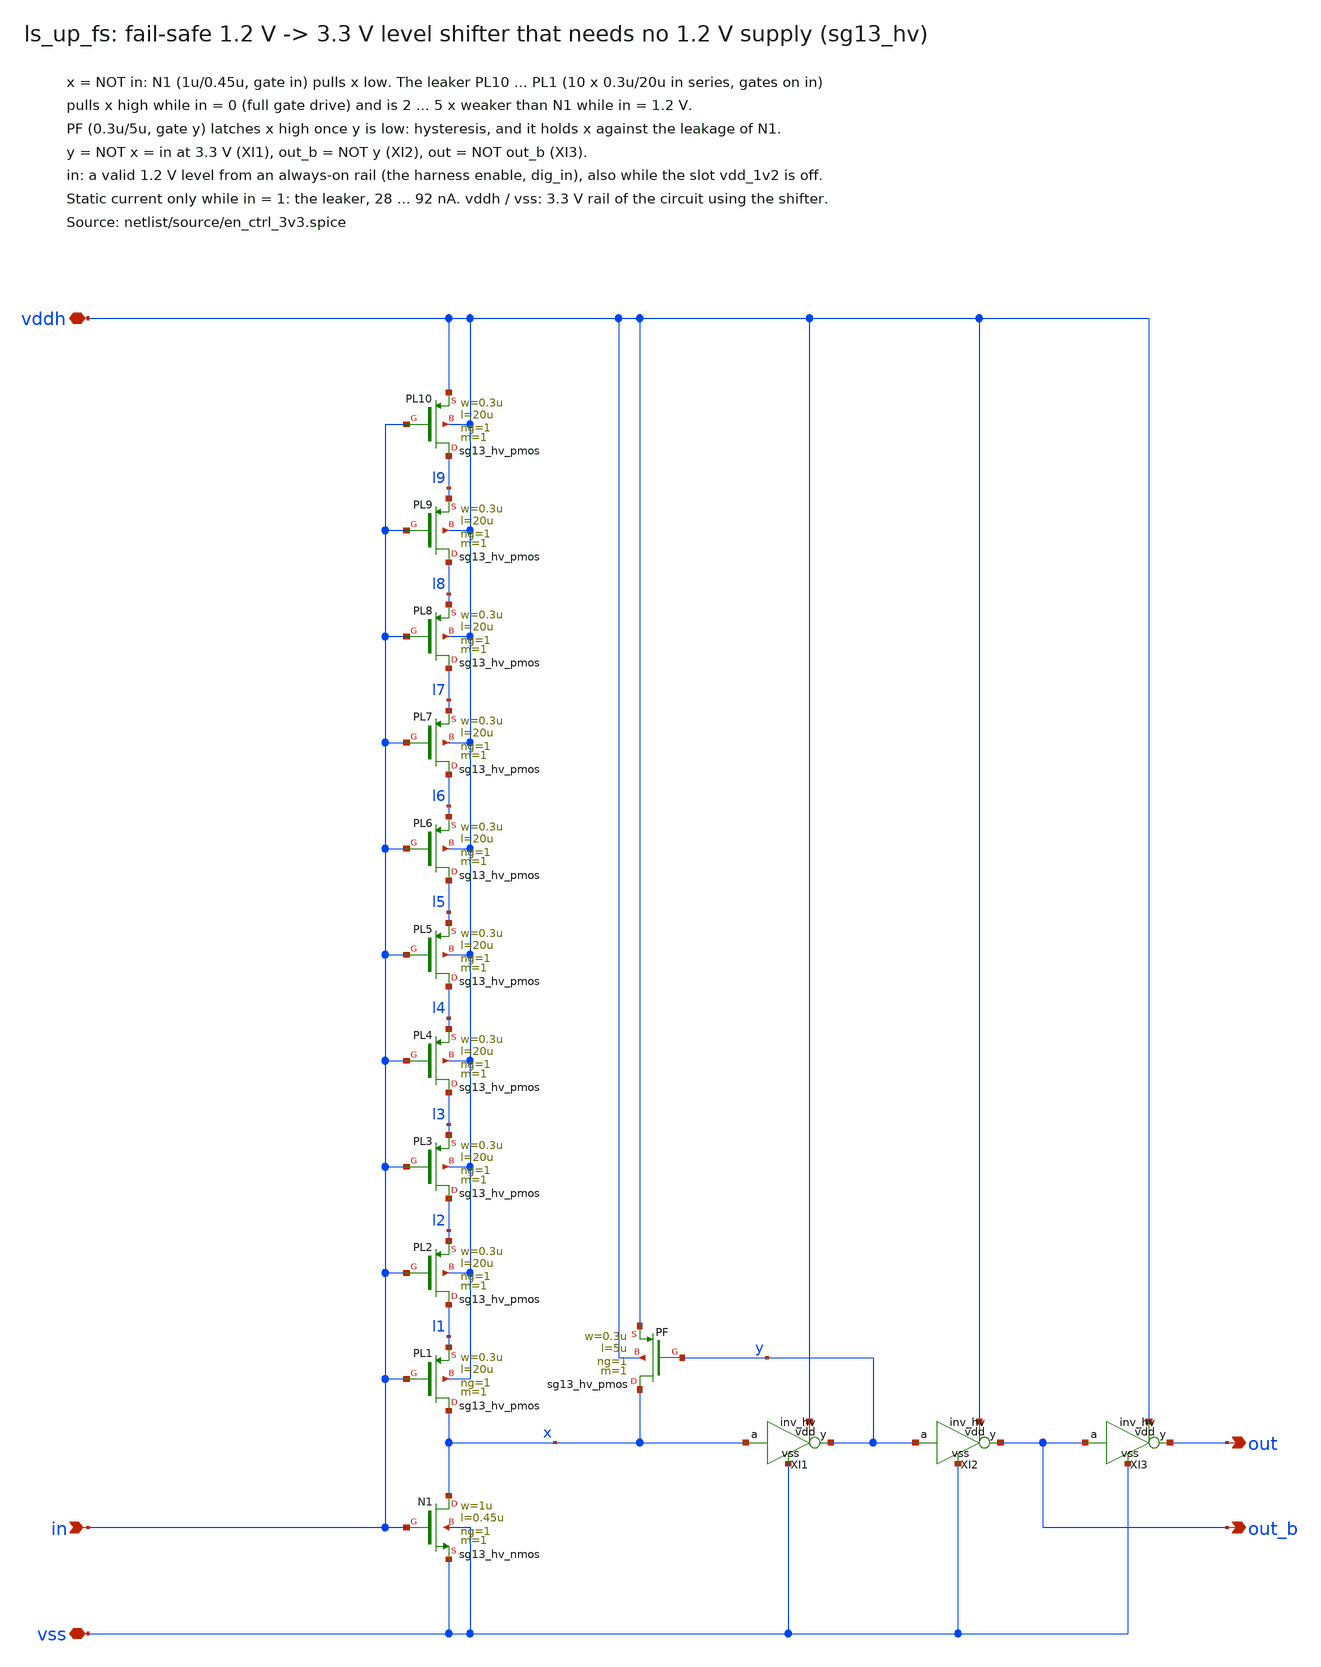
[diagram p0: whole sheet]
** sch_path: macros/en_ctrl_3v3/schematic/xschem/ls_up_fs.sch
**.subckt ls_up_fs vddh vss in out out_b
*.iopin vddh
*.iopin vss
*.ipin in
*.opin out
*.opin out_b
XN1 x in vss vss sg13_hv_nmos w=1u l=0.45u ng=1 m=1 mm_ok=1
XPL10 l9 in vddh vddh sg13_hv_pmos w=0.3u l=20u ng=1 m=1 mm_ok=1
XPL9 l8 in l9 vddh sg13_hv_pmos w=0.3u l=20u ng=1 m=1 mm_ok=1
XPL8 l7 in l8 vddh sg13_hv_pmos w=0.3u l=20u ng=1 m=1 mm_ok=1
XPL7 l6 in l7 vddh sg13_hv_pmos w=0.3u l=20u ng=1 m=1 mm_ok=1
XPL6 l5 in l6 vddh sg13_hv_pmos w=0.3u l=20u ng=1 m=1 mm_ok=1
XPL5 l4 in l5 vddh sg13_hv_pmos w=0.3u l=20u ng=1 m=1 mm_ok=1
XPL4 l3 in l4 vddh sg13_hv_pmos w=0.3u l=20u ng=1 m=1 mm_ok=1
XPL3 l2 in l3 vddh sg13_hv_pmos w=0.3u l=20u ng=1 m=1 mm_ok=1
XPL2 l1 in l2 vddh sg13_hv_pmos w=0.3u l=20u ng=1 m=1 mm_ok=1
XPL1 x in l1 vddh sg13_hv_pmos w=0.3u l=20u ng=1 m=1 mm_ok=1
XPF x y vddh vddh sg13_hv_pmos w=0.3u l=5u ng=1 m=1 mm_ok=1
XI1 vddh vss x y inv_hv
XI2 vddh vss y out_b inv_hv
XI3 vddh vss out_b out inv_hv
**.ends

* expanding   symbol:  inv_hv.sym # of pins=4
** sym_path: macros/hv_logic/schematic/xschem/inv_hv.sym
** sch_path: macros/hv_logic/schematic/xschem/inv_hv.sch
.subckt inv_hv vdd vss a y
*.iopin vdd
*.iopin vss
*.ipin a
*.opin y
XP y a vdd vdd sg13_hv_pmos w=1u l=0.45u ng=1 m=1 mm_ok=1
XN y a vss vss sg13_hv_nmos w=1u l=0.45u ng=1 m=1 mm_ok=1
.ends

.end
